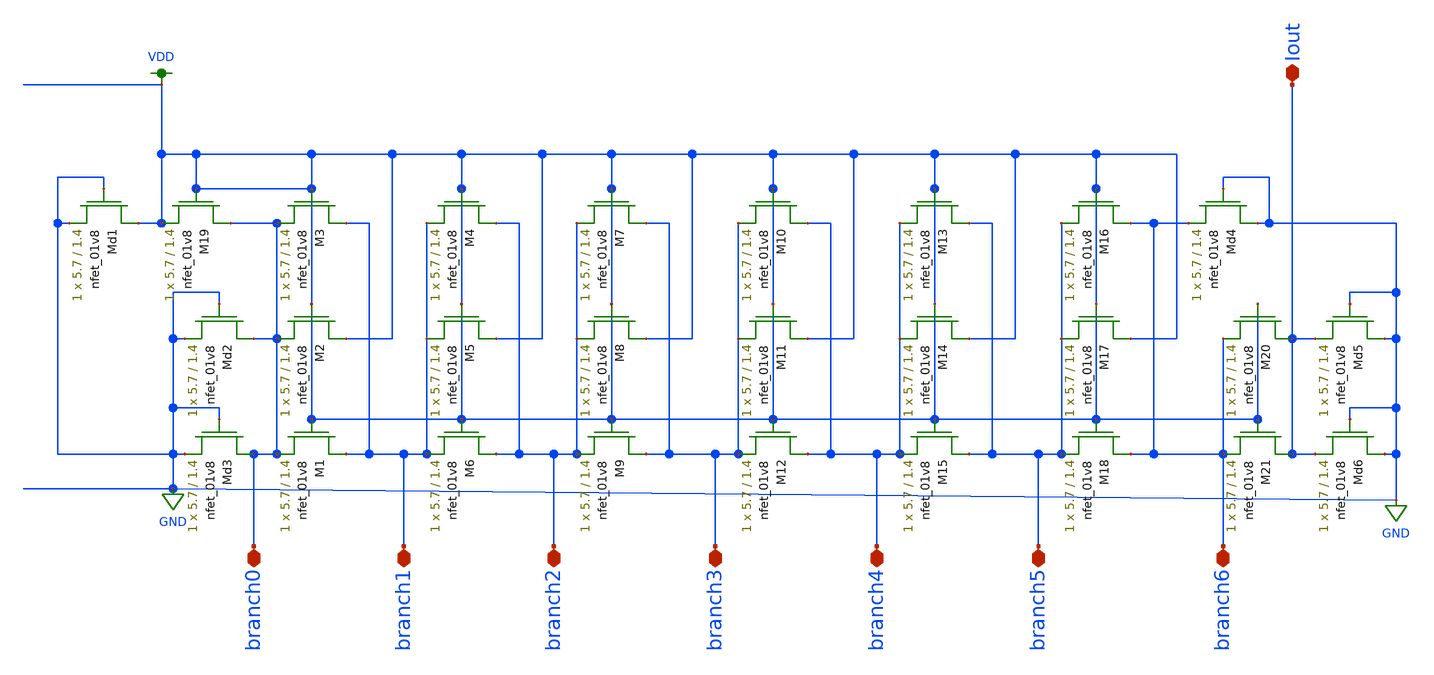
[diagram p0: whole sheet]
** sch_path: design-files/dacladder.sch
**.subckt dacladder branch0 branch1 branch2 branch3 branch4 branch5 branch6 Iout
*.iopin branch0
*.iopin branch1
*.iopin branch2
*.iopin branch3
*.iopin branch4
*.iopin branch5
*.iopin branch6
*.iopin Iout
XM19 branch0 VDD VDD GND sky130_fd_pr__nfet_01v8 L=1.4 W=5.7 nf=1 ad='int((nf+1)/2) * W/nf * 0.29' as='int((nf+2)/2) * W/nf * 0.29'
+ pd='2*int((nf+1)/2) * (W/nf + 0.29)' ps='2*int((nf+2)/2) * (W/nf + 0.29)' nrd='0.29 / W' nrs='0.29 / W'
+ sa=0 sb=0 sd=0 mult=1 m=1
XM3 branch1 VDD branch0 GND sky130_fd_pr__nfet_01v8 L=1.4 W=5.7 nf=1 ad='int((nf+1)/2) * W/nf * 0.29'
+ as='int((nf+2)/2) * W/nf * 0.29' pd='2*int((nf+1)/2) * (W/nf + 0.29)' ps='2*int((nf+2)/2) * (W/nf + 0.29)'
+ nrd='0.29 / W' nrs='0.29 / W' sa=0 sb=0 sd=0 mult=1 m=1
XM2 VDD VDD branch0 GND sky130_fd_pr__nfet_01v8 L=1.4 W=5.7 nf=1 ad='int((nf+1)/2) * W/nf * 0.29' as='int((nf+2)/2) * W/nf * 0.29'
+ pd='2*int((nf+1)/2) * (W/nf + 0.29)' ps='2*int((nf+2)/2) * (W/nf + 0.29)' nrd='0.29 / W' nrs='0.29 / W'
+ sa=0 sb=0 sd=0 mult=1 m=1
XM1 branch1 VDD branch0 GND sky130_fd_pr__nfet_01v8 L=1.4 W=5.7 nf=1 ad='int((nf+1)/2) * W/nf * 0.29'
+ as='int((nf+2)/2) * W/nf * 0.29' pd='2*int((nf+1)/2) * (W/nf + 0.29)' ps='2*int((nf+2)/2) * (W/nf + 0.29)'
+ nrd='0.29 / W' nrs='0.29 / W' sa=0 sb=0 sd=0 mult=1 m=1
XM4 branch2 VDD branch1 GND sky130_fd_pr__nfet_01v8 L=1.4 W=5.7 nf=1 ad='int((nf+1)/2) * W/nf * 0.29'
+ as='int((nf+2)/2) * W/nf * 0.29' pd='2*int((nf+1)/2) * (W/nf + 0.29)' ps='2*int((nf+2)/2) * (W/nf + 0.29)'
+ nrd='0.29 / W' nrs='0.29 / W' sa=0 sb=0 sd=0 mult=1 m=1
XM5 VDD VDD branch1 GND sky130_fd_pr__nfet_01v8 L=1.4 W=5.7 nf=1 ad='int((nf+1)/2) * W/nf * 0.29' as='int((nf+2)/2) * W/nf * 0.29'
+ pd='2*int((nf+1)/2) * (W/nf + 0.29)' ps='2*int((nf+2)/2) * (W/nf + 0.29)' nrd='0.29 / W' nrs='0.29 / W'
+ sa=0 sb=0 sd=0 mult=1 m=1
XM6 branch2 VDD branch1 GND sky130_fd_pr__nfet_01v8 L=1.4 W=5.7 nf=1 ad='int((nf+1)/2) * W/nf * 0.29'
+ as='int((nf+2)/2) * W/nf * 0.29' pd='2*int((nf+1)/2) * (W/nf + 0.29)' ps='2*int((nf+2)/2) * (W/nf + 0.29)'
+ nrd='0.29 / W' nrs='0.29 / W' sa=0 sb=0 sd=0 mult=1 m=1
XM7 branch3 VDD branch2 GND sky130_fd_pr__nfet_01v8 L=1.4 W=5.7 nf=1 ad='int((nf+1)/2) * W/nf * 0.29'
+ as='int((nf+2)/2) * W/nf * 0.29' pd='2*int((nf+1)/2) * (W/nf + 0.29)' ps='2*int((nf+2)/2) * (W/nf + 0.29)'
+ nrd='0.29 / W' nrs='0.29 / W' sa=0 sb=0 sd=0 mult=1 m=1
XM8 VDD VDD branch2 GND sky130_fd_pr__nfet_01v8 L=1.4 W=5.7 nf=1 ad='int((nf+1)/2) * W/nf * 0.29' as='int((nf+2)/2) * W/nf * 0.29'
+ pd='2*int((nf+1)/2) * (W/nf + 0.29)' ps='2*int((nf+2)/2) * (W/nf + 0.29)' nrd='0.29 / W' nrs='0.29 / W'
+ sa=0 sb=0 sd=0 mult=1 m=1
XM9 branch3 VDD branch2 GND sky130_fd_pr__nfet_01v8 L=1.4 W=5.7 nf=1 ad='int((nf+1)/2) * W/nf * 0.29'
+ as='int((nf+2)/2) * W/nf * 0.29' pd='2*int((nf+1)/2) * (W/nf + 0.29)' ps='2*int((nf+2)/2) * (W/nf + 0.29)'
+ nrd='0.29 / W' nrs='0.29 / W' sa=0 sb=0 sd=0 mult=1 m=1
XM10 branch4 VDD branch3 GND sky130_fd_pr__nfet_01v8 L=1.4 W=5.7 nf=1 ad='int((nf+1)/2) * W/nf * 0.29'
+ as='int((nf+2)/2) * W/nf * 0.29' pd='2*int((nf+1)/2) * (W/nf + 0.29)' ps='2*int((nf+2)/2) * (W/nf + 0.29)'
+ nrd='0.29 / W' nrs='0.29 / W' sa=0 sb=0 sd=0 mult=1 m=1
XM11 VDD VDD branch3 GND sky130_fd_pr__nfet_01v8 L=1.4 W=5.7 nf=1 ad='int((nf+1)/2) * W/nf * 0.29' as='int((nf+2)/2) * W/nf * 0.29'
+ pd='2*int((nf+1)/2) * (W/nf + 0.29)' ps='2*int((nf+2)/2) * (W/nf + 0.29)' nrd='0.29 / W' nrs='0.29 / W'
+ sa=0 sb=0 sd=0 mult=1 m=1
XM12 branch4 VDD branch3 GND sky130_fd_pr__nfet_01v8 L=1.4 W=5.7 nf=1 ad='int((nf+1)/2) * W/nf * 0.29'
+ as='int((nf+2)/2) * W/nf * 0.29' pd='2*int((nf+1)/2) * (W/nf + 0.29)' ps='2*int((nf+2)/2) * (W/nf + 0.29)'
+ nrd='0.29 / W' nrs='0.29 / W' sa=0 sb=0 sd=0 mult=1 m=1
XM13 branch5 VDD branch4 GND sky130_fd_pr__nfet_01v8 L=1.4 W=5.7 nf=1 ad='int((nf+1)/2) * W/nf * 0.29'
+ as='int((nf+2)/2) * W/nf * 0.29' pd='2*int((nf+1)/2) * (W/nf + 0.29)' ps='2*int((nf+2)/2) * (W/nf + 0.29)'
+ nrd='0.29 / W' nrs='0.29 / W' sa=0 sb=0 sd=0 mult=1 m=1
XM14 VDD VDD branch4 GND sky130_fd_pr__nfet_01v8 L=1.4 W=5.7 nf=1 ad='int((nf+1)/2) * W/nf * 0.29' as='int((nf+2)/2) * W/nf * 0.29'
+ pd='2*int((nf+1)/2) * (W/nf + 0.29)' ps='2*int((nf+2)/2) * (W/nf + 0.29)' nrd='0.29 / W' nrs='0.29 / W'
+ sa=0 sb=0 sd=0 mult=1 m=1
XM15 branch5 VDD branch4 GND sky130_fd_pr__nfet_01v8 L=1.4 W=5.7 nf=1 ad='int((nf+1)/2) * W/nf * 0.29'
+ as='int((nf+2)/2) * W/nf * 0.29' pd='2*int((nf+1)/2) * (W/nf + 0.29)' ps='2*int((nf+2)/2) * (W/nf + 0.29)'
+ nrd='0.29 / W' nrs='0.29 / W' sa=0 sb=0 sd=0 mult=1 m=1
XM16 branch6 VDD branch5 GND sky130_fd_pr__nfet_01v8 L=1.4 W=5.7 nf=1 ad='int((nf+1)/2) * W/nf * 0.29'
+ as='int((nf+2)/2) * W/nf * 0.29' pd='2*int((nf+1)/2) * (W/nf + 0.29)' ps='2*int((nf+2)/2) * (W/nf + 0.29)'
+ nrd='0.29 / W' nrs='0.29 / W' sa=0 sb=0 sd=0 mult=1 m=1
XM17 VDD VDD branch5 GND sky130_fd_pr__nfet_01v8 L=1.4 W=5.7 nf=1 ad='int((nf+1)/2) * W/nf * 0.29' as='int((nf+2)/2) * W/nf * 0.29'
+ pd='2*int((nf+1)/2) * (W/nf + 0.29)' ps='2*int((nf+2)/2) * (W/nf + 0.29)' nrd='0.29 / W' nrs='0.29 / W'
+ sa=0 sb=0 sd=0 mult=1 m=1
XM18 branch6 VDD branch5 GND sky130_fd_pr__nfet_01v8 L=1.4 W=5.7 nf=1 ad='int((nf+1)/2) * W/nf * 0.29'
+ as='int((nf+2)/2) * W/nf * 0.29' pd='2*int((nf+1)/2) * (W/nf + 0.29)' ps='2*int((nf+2)/2) * (W/nf + 0.29)'
+ nrd='0.29 / W' nrs='0.29 / W' sa=0 sb=0 sd=0 mult=1 m=1
XMd4 GND GND branch6 GND sky130_fd_pr__nfet_01v8 L=1.4 W=5.7 nf=1 ad='int((nf+1)/2) * W/nf * 0.29' as='int((nf+2)/2) * W/nf * 0.29'
+ pd='2*int((nf+1)/2) * (W/nf + 0.29)' ps='2*int((nf+2)/2) * (W/nf + 0.29)' nrd='0.29 / W' nrs='0.29 / W'
+ sa=0 sb=0 sd=0 mult=1 m=1
XM20 Iout VDD branch6 GND sky130_fd_pr__nfet_01v8 L=1.4 W=5.7 nf=1 ad='int((nf+1)/2) * W/nf * 0.29' as='int((nf+2)/2) * W/nf * 0.29'
+ pd='2*int((nf+1)/2) * (W/nf + 0.29)' ps='2*int((nf+2)/2) * (W/nf + 0.29)' nrd='0.29 / W' nrs='0.29 / W'
+ sa=0 sb=0 sd=0 mult=1 m=1
XM21 Iout VDD branch6 GND sky130_fd_pr__nfet_01v8 L=1.4 W=5.7 nf=1 ad='int((nf+1)/2) * W/nf * 0.29' as='int((nf+2)/2) * W/nf * 0.29'
+ pd='2*int((nf+1)/2) * (W/nf + 0.29)' ps='2*int((nf+2)/2) * (W/nf + 0.29)' nrd='0.29 / W' nrs='0.29 / W'
+ sa=0 sb=0 sd=0 mult=1 m=1
XMd6 GND GND Iout GND sky130_fd_pr__nfet_01v8 L=1.4 W=5.7 nf=1 ad='int((nf+1)/2) * W/nf * 0.29' as='int((nf+2)/2) * W/nf * 0.29'
+ pd='2*int((nf+1)/2) * (W/nf + 0.29)' ps='2*int((nf+2)/2) * (W/nf + 0.29)' nrd='0.29 / W' nrs='0.29 / W'
+ sa=0 sb=0 sd=0 mult=1 m=1
XMd5 GND GND Iout GND sky130_fd_pr__nfet_01v8 L=1.4 W=5.7 nf=1 ad='int((nf+1)/2) * W/nf * 0.29' as='int((nf+2)/2) * W/nf * 0.29'
+ pd='2*int((nf+1)/2) * (W/nf + 0.29)' ps='2*int((nf+2)/2) * (W/nf + 0.29)' nrd='0.29 / W' nrs='0.29 / W'
+ sa=0 sb=0 sd=0 mult=1 m=1
XMd3 branch0 GND GND GND sky130_fd_pr__nfet_01v8 L=1.4 W=5.7 nf=1 ad='int((nf+1)/2) * W/nf * 0.29' as='int((nf+2)/2) * W/nf * 0.29'
+ pd='2*int((nf+1)/2) * (W/nf + 0.29)' ps='2*int((nf+2)/2) * (W/nf + 0.29)' nrd='0.29 / W' nrs='0.29 / W'
+ sa=0 sb=0 sd=0 mult=1 m=1
XMd2 branch0 GND GND GND sky130_fd_pr__nfet_01v8 L=1.4 W=5.7 nf=1 ad='int((nf+1)/2) * W/nf * 0.29' as='int((nf+2)/2) * W/nf * 0.29'
+ pd='2*int((nf+1)/2) * (W/nf + 0.29)' ps='2*int((nf+2)/2) * (W/nf + 0.29)' nrd='0.29 / W' nrs='0.29 / W'
+ sa=0 sb=0 sd=0 mult=1 m=1
XMd1 VDD GND GND GND sky130_fd_pr__nfet_01v8 L=1.4 W=5.7 nf=1 ad='int((nf+1)/2) * W/nf * 0.29' as='int((nf+2)/2) * W/nf * 0.29'
+ pd='2*int((nf+1)/2) * (W/nf + 0.29)' ps='2*int((nf+2)/2) * (W/nf + 0.29)' nrd='0.29 / W' nrs='0.29 / W'
+ sa=0 sb=0 sd=0 mult=1 m=1
**.ends
.GLOBAL VDD
.GLOBAL GND
.end
